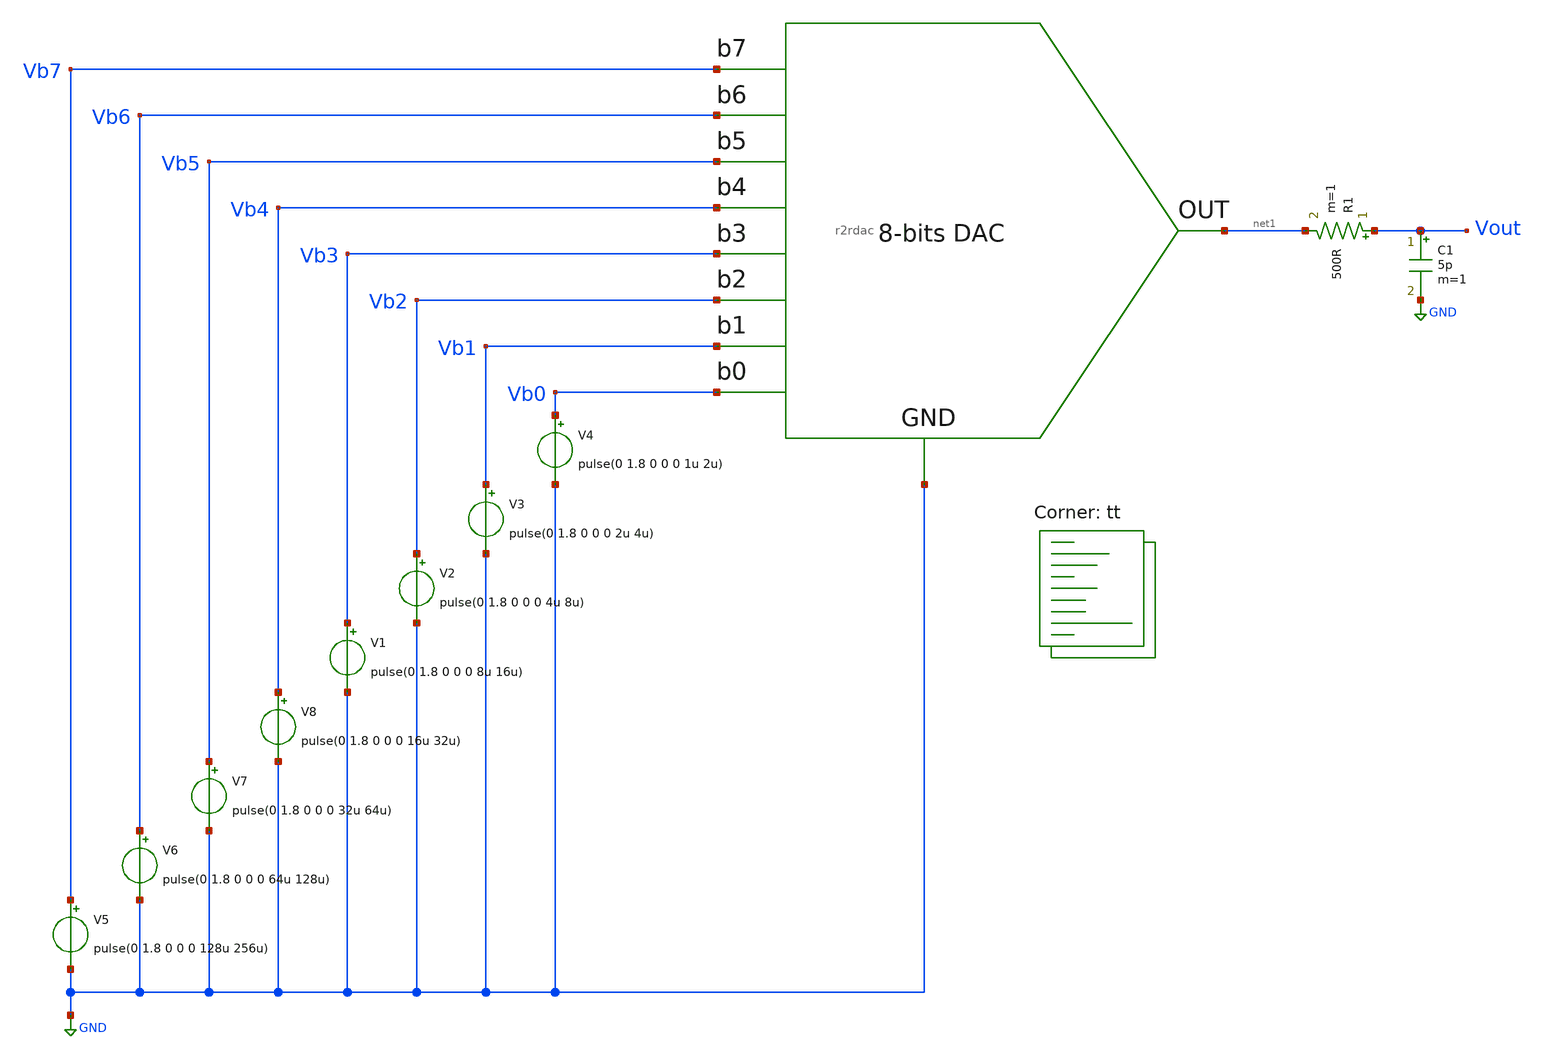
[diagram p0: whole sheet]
** sch_path: xschem/r2rdac_tb.sch
**.subckt r2rdac_tb
X1 Vb0 Vb1 Vb2 Vb3 Vb4 Vb5 Vb6 Vb7 GND net1 r2rdac
V1 Vb3 GND pulse(0 1.8 0 0 0 8u 16u)
V2 Vb2 GND pulse(0 1.8 0 0 0 4u 8u)
V3 Vb1 GND pulse(0 1.8 0 0 0 2u 4u)
V4 Vb0 GND pulse(0 1.8 0 0 0 1u 2u)
V5 Vb7 GND pulse(0 1.8 0 0 0 128u 256u)
V6 Vb6 GND pulse(0 1.8 0 0 0 64u 128u)
V7 Vb5 GND pulse(0 1.8 0 0 0 32u 64u)
V8 Vb4 GND pulse(0 1.8 0 0 0 16u 32u)
R1 Vout net1 500R m=1
C1 Vout GND 5p m=1
**** begin user architecture code


* .options filetype=ascii
.control
tran 10n 256u uic
write r2rdac_tb.raw
.endc
.end


.lib $::SKYWATER_MODELS/sky130.lib.spice tt
**** end user architecture code
**.ends

* expanding   symbol:  r2rdac.sym # of pins=10
** sym_path: xschem/r2rdac.sym
** sch_path: xschem/r2rdac.sch
.subckt r2rdac b0 b1 b2 b3 b4 b5 b6 b7 GND OUT
*.ipin b7
*.ipin b6
*.ipin b5
*.ipin b4
*.ipin b3
*.ipin b2
*.ipin b1
*.ipin b0
*.ipin GND
*.opin OUT
XR16 b7 OUT GND sky130_fd_pr__res_high_po_0p35 L=40 mult=1 m=1
XR2 b6 net1 GND sky130_fd_pr__res_high_po_0p35 L=40 mult=1 m=1
XR3 b5 net2 GND sky130_fd_pr__res_high_po_0p35 L=40 mult=1 m=1
XR4 b4 net3 GND sky130_fd_pr__res_high_po_0p35 L=40 mult=1 m=1
XR5 b3 net4 GND sky130_fd_pr__res_high_po_0p35 L=40 mult=1 m=1
XR6 b2 net5 GND sky130_fd_pr__res_high_po_0p35 L=40 mult=1 m=1
XR7 b1 net6 GND sky130_fd_pr__res_high_po_0p35 L=40 mult=1 m=1
XR8 b0 net7 GND sky130_fd_pr__res_high_po_0p35 L=40 mult=1 m=1
XR1 GND net7 GND sky130_fd_pr__res_high_po_0p35 L=40 mult=1 m=1
XR9 net7 net6 GND sky130_fd_pr__res_high_po_0p35 L=20 mult=1 m=1
XR10 net6 net5 GND sky130_fd_pr__res_high_po_0p35 L=20 mult=1 m=1
XR11 net5 net4 GND sky130_fd_pr__res_high_po_0p35 L=20 mult=1 m=1
XR12 net4 net3 GND sky130_fd_pr__res_high_po_0p35 L=20 mult=1 m=1
XR13 net3 net2 GND sky130_fd_pr__res_high_po_0p35 L=20 mult=1 m=1
XR14 net2 net1 GND sky130_fd_pr__res_high_po_0p35 L=20 mult=1 m=1
XR15 net1 OUT GND sky130_fd_pr__res_high_po_0p35 L=20 mult=1 m=1
.ends

.GLOBAL GND
.end
